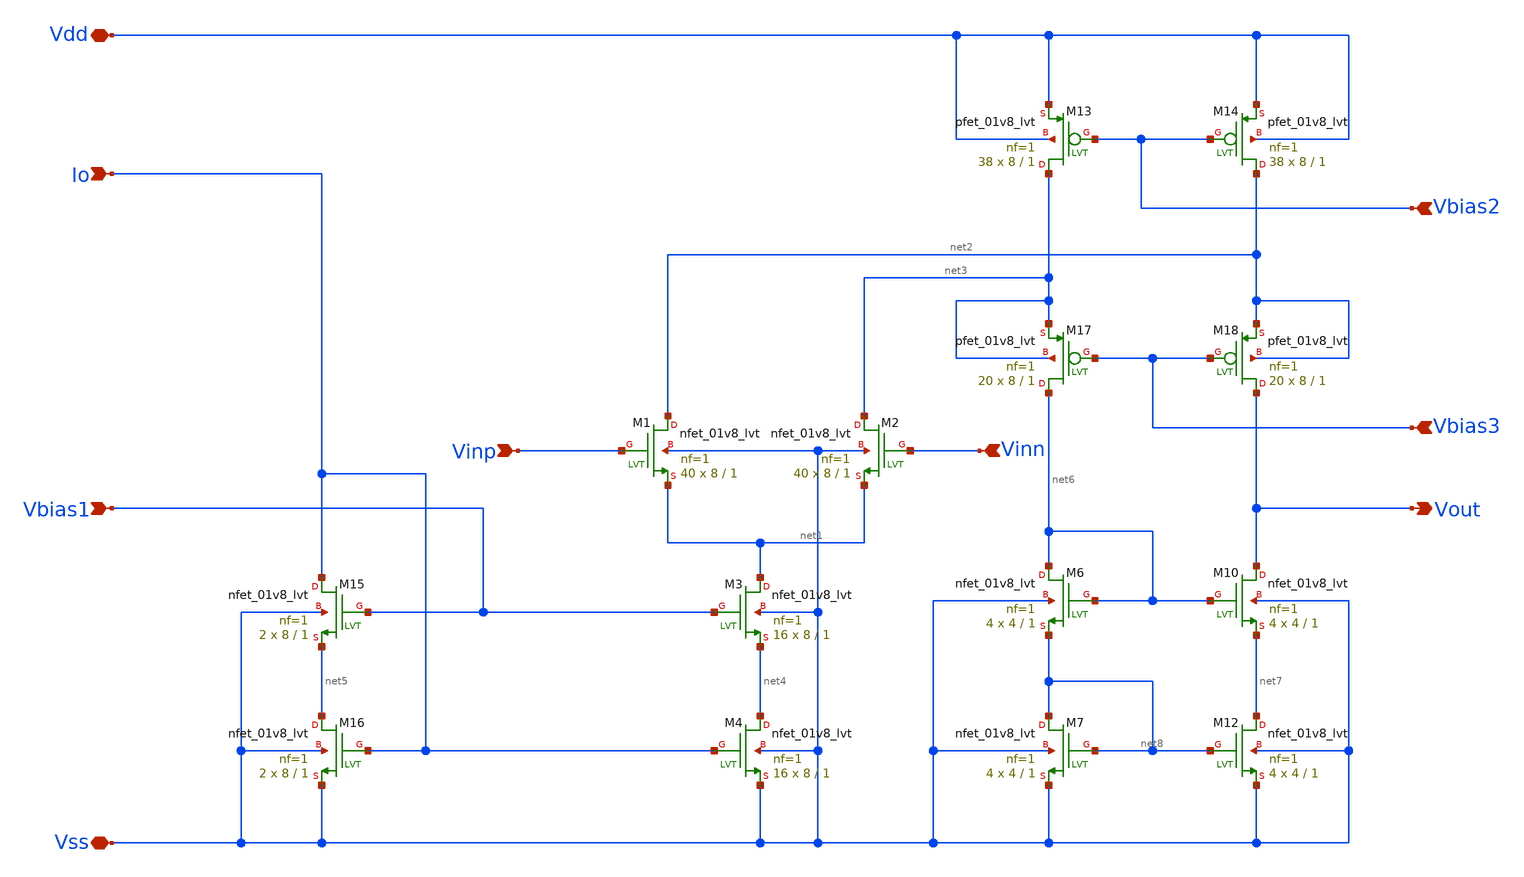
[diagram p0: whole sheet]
** sch_path: xschem/ip_block/opamp/folded_cas_xiaoyi/test_output_driver.sch
**.subckt test_output_driver Io Vbias1 Vinp Vinn Vbias2 Vbias3 Vout Vdd Vss
*.ipin Io
*.ipin Vbias1
*.ipin Vinp
*.ipin Vinn
*.ipin Vbias2
*.ipin Vbias3
*.opin Vout
*.iopin Vdd
*.iopin Vss
XM1 net2 Vinp net1 Vss sky130_fd_pr__nfet_01v8_lvt L=1 W=8 nf=1 ad='int((nf+1)/2) * W/nf * 0.29' as='int((nf+2)/2) * W/nf * 0.29'
+ pd='2*int((nf+1)/2) * (W/nf + 0.29)' ps='2*int((nf+2)/2) * (W/nf + 0.29)' nrd='0.29 / W' nrs='0.29 / W'
+ sa=0 sb=0 sd=0 mult=40 m=40
XM2 net3 Vinn net1 Vss sky130_fd_pr__nfet_01v8_lvt L=1 W=8 nf=1 ad='int((nf+1)/2) * W/nf * 0.29' as='int((nf+2)/2) * W/nf * 0.29'
+ pd='2*int((nf+1)/2) * (W/nf + 0.29)' ps='2*int((nf+2)/2) * (W/nf + 0.29)' nrd='0.29 / W' nrs='0.29 / W'
+ sa=0 sb=0 sd=0 mult=40 m=40
XM3 net1 Vbias1 net4 Vss sky130_fd_pr__nfet_01v8_lvt L=1 W=8 nf=1 ad='int((nf+1)/2) * W/nf * 0.29' as='int((nf+2)/2) * W/nf * 0.29'
+ pd='2*int((nf+1)/2) * (W/nf + 0.29)' ps='2*int((nf+2)/2) * (W/nf + 0.29)' nrd='0.29 / W' nrs='0.29 / W'
+ sa=0 sb=0 sd=0 mult=16 m=16
XM4 net4 Io Vss Vss sky130_fd_pr__nfet_01v8_lvt L=1 W=8 nf=1 ad='int((nf+1)/2) * W/nf * 0.29' as='int((nf+2)/2) * W/nf * 0.29'
+ pd='2*int((nf+1)/2) * (W/nf + 0.29)' ps='2*int((nf+2)/2) * (W/nf + 0.29)' nrd='0.29 / W' nrs='0.29 / W'
+ sa=0 sb=0 sd=0 mult=16 m=16
XM10 Vout net6 net7 Vss sky130_fd_pr__nfet_01v8_lvt L=1 W=4 nf=1 ad='int((nf+1)/2) * W/nf * 0.29' as='int((nf+2)/2) * W/nf * 0.29'
+ pd='2*int((nf+1)/2) * (W/nf + 0.29)' ps='2*int((nf+2)/2) * (W/nf + 0.29)' nrd='0.29 / W' nrs='0.29 / W'
+ sa=0 sb=0 sd=0 mult=4 m=4
XM12 net7 net8 Vss Vss sky130_fd_pr__nfet_01v8_lvt L=1 W=4 nf=1 ad='int((nf+1)/2) * W/nf * 0.29' as='int((nf+2)/2) * W/nf * 0.29'
+ pd='2*int((nf+1)/2) * (W/nf + 0.29)' ps='2*int((nf+2)/2) * (W/nf + 0.29)' nrd='0.29 / W' nrs='0.29 / W'
+ sa=0 sb=0 sd=0 mult=4 m=4
XM15 Io Vbias1 net5 Vss sky130_fd_pr__nfet_01v8_lvt L=1 W=8 nf=1 ad='int((nf+1)/2) * W/nf * 0.29' as='int((nf+2)/2) * W/nf * 0.29'
+ pd='2*int((nf+1)/2) * (W/nf + 0.29)' ps='2*int((nf+2)/2) * (W/nf + 0.29)' nrd='0.29 / W' nrs='0.29 / W'
+ sa=0 sb=0 sd=0 mult=2 m=2
XM16 net5 Io Vss Vss sky130_fd_pr__nfet_01v8_lvt L=1 W=8 nf=1 ad='int((nf+1)/2) * W/nf * 0.29' as='int((nf+2)/2) * W/nf * 0.29'
+ pd='2*int((nf+1)/2) * (W/nf + 0.29)' ps='2*int((nf+2)/2) * (W/nf + 0.29)' nrd='0.29 / W' nrs='0.29 / W'
+ sa=0 sb=0 sd=0 mult=2 m=2
XM13 net3 Vbias2 Vdd Vdd sky130_fd_pr__pfet_01v8_lvt L=1 W=8 nf=1 ad='int((nf+1)/2) * W/nf * 0.29' as='int((nf+2)/2) * W/nf * 0.29'
+ pd='2*int((nf+1)/2) * (W/nf + 0.29)' ps='2*int((nf+2)/2) * (W/nf + 0.29)' nrd='0.29 / W' nrs='0.29 / W'
+ sa=0 sb=0 sd=0 mult=38 m=38
XM14 net2 Vbias2 Vdd Vdd sky130_fd_pr__pfet_01v8_lvt L=1 W=8 nf=1 ad='int((nf+1)/2) * W/nf * 0.29' as='int((nf+2)/2) * W/nf * 0.29'
+ pd='2*int((nf+1)/2) * (W/nf + 0.29)' ps='2*int((nf+2)/2) * (W/nf + 0.29)' nrd='0.29 / W' nrs='0.29 / W'
+ sa=0 sb=0 sd=0 mult=38 m=38
XM17 net6 Vbias3 net3 net3 sky130_fd_pr__pfet_01v8_lvt L=1 W=8 nf=1 ad='int((nf+1)/2) * W/nf * 0.29'
+ as='int((nf+2)/2) * W/nf * 0.29' pd='2*int((nf+1)/2) * (W/nf + 0.29)' ps='2*int((nf+2)/2) * (W/nf + 0.29)'
+ nrd='0.29 / W' nrs='0.29 / W' sa=0 sb=0 sd=0 mult=20 m=20
XM18 Vout Vbias3 net2 net2 sky130_fd_pr__pfet_01v8_lvt L=1 W=8 nf=1 ad='int((nf+1)/2) * W/nf * 0.29'
+ as='int((nf+2)/2) * W/nf * 0.29' pd='2*int((nf+1)/2) * (W/nf + 0.29)' ps='2*int((nf+2)/2) * (W/nf + 0.29)'
+ nrd='0.29 / W' nrs='0.29 / W' sa=0 sb=0 sd=0 mult=20 m=20
XM6 net6 net6 net8 Vss sky130_fd_pr__nfet_01v8_lvt L=1 W=4 nf=1 ad='int((nf+1)/2) * W/nf * 0.29' as='int((nf+2)/2) * W/nf * 0.29'
+ pd='2*int((nf+1)/2) * (W/nf + 0.29)' ps='2*int((nf+2)/2) * (W/nf + 0.29)' nrd='0.29 / W' nrs='0.29 / W'
+ sa=0 sb=0 sd=0 mult=4 m=4
XM7 net8 net8 Vss Vss sky130_fd_pr__nfet_01v8_lvt L=1 W=4 nf=1 ad='int((nf+1)/2) * W/nf * 0.29' as='int((nf+2)/2) * W/nf * 0.29'
+ pd='2*int((nf+1)/2) * (W/nf + 0.29)' ps='2*int((nf+2)/2) * (W/nf + 0.29)' nrd='0.29 / W' nrs='0.29 / W'
+ sa=0 sb=0 sd=0 mult=4 m=4
**.ends
.end
